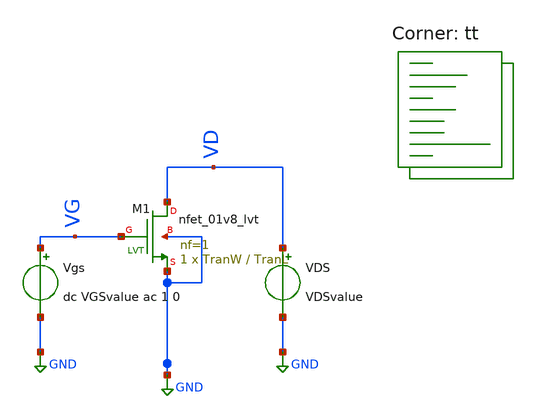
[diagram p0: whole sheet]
** sch_path: Schematics/NMOSlvtchar.sch
**.subckt NMOSlvtchar
Vgs VG GND dc VGSvalue ac 1 0
VDS VD GND VDSvalue
XM1 VD VG GND GND sky130_fd_pr__nfet_01v8_lvt L=TranL W=TranW nf=1 ad='int((nf+1)/2) * W/nf * 0.29' as='int((nf+2)/2) * W/nf * 0.29'
+ pd='2*int((nf+1)/2) * (W/nf + 0.29)' ps='2*int((nf+2)/2) * (W/nf + 0.29)' nrd='0.29 / W' nrs='0.29 / W'
+ sa=0 sb=0 sd=0 mult=1 m=1
**** begin user architecture code
.lib $::SKYWATER_MODELS/sky130.lib.spice tt
**** end user architecture code
**.ends
.GLOBAL GND
.end
